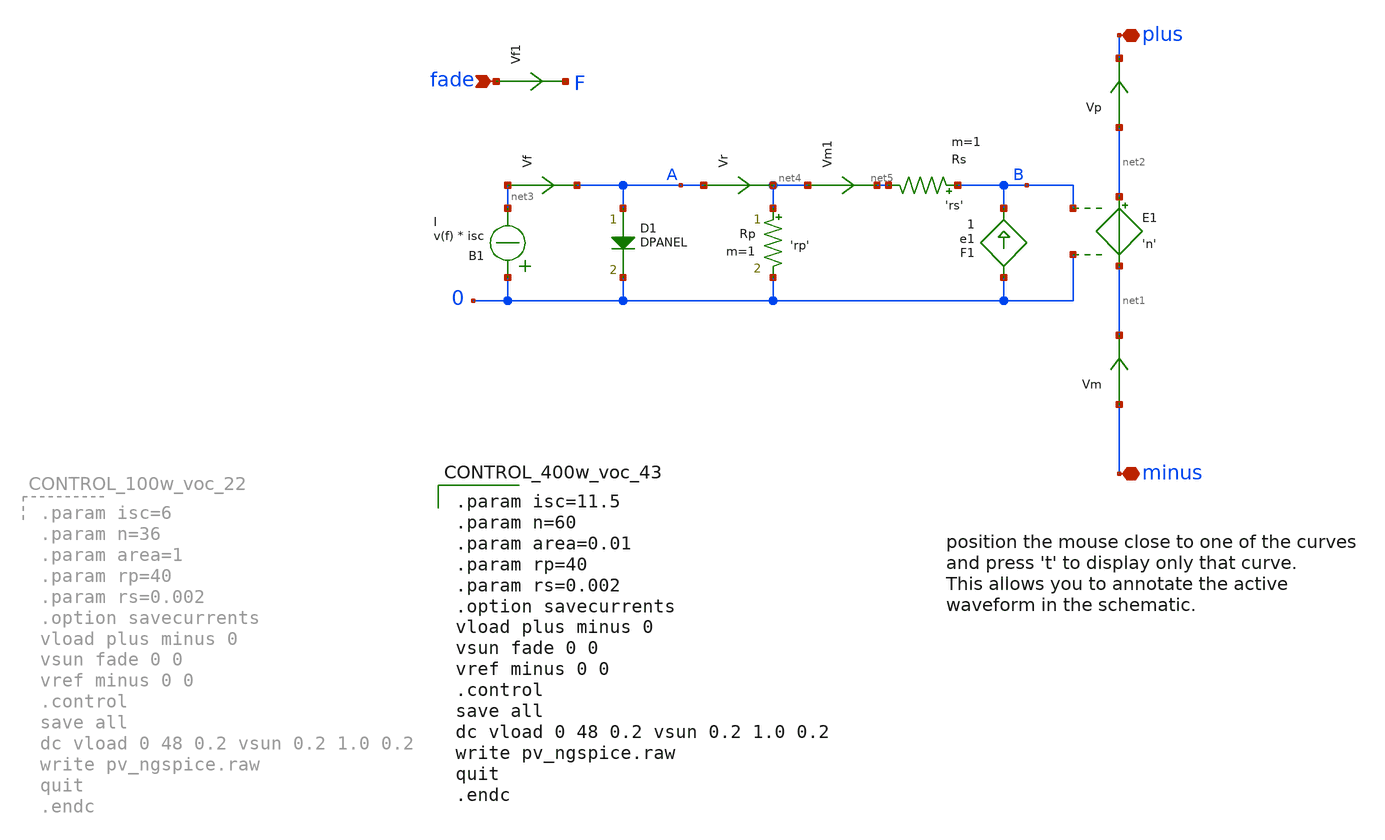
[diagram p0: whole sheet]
** sch_path: xschem_library/ngspice/pv_ngspice.sch
* Copyright (C) 1998-2023 Stefan Frederik Schippers
* This program is free software; you can redistribute it and/or modify
* it under the terms of the GNU General Public License as published by
* the Free Software Foundation; either version 2 of the License, or
* (at your option) any later version.
* This program is distributed in the hope that it will be useful,
* but WITHOUT ANY WARRANTY; without even the implied warranty of
* MERCHANTABILITY or FITNESS FOR A PARTICULAR PURPOSE.  See the
* GNU General Public License for more details.
* You should have received a copy of the GNU General Public License
* along with this program; if not, write to the Free Software
**.subckt pv_ngspice minus fade plus
*.iopin minus
*.ipin fade
*.iopin plus
Vf net3 A 0
.save i(vf)
Vm minus net1 0
.save i(vm)
Vp net2 plus 0
.save i(vp)
D1 A 0 DPANEL area='area'
Rp net4 0 'rp' m=1
Rs B net5 'rs' m=1
F1 0 B e1 1
E1 net2 net1 B 0 'n'
Vf1 fade F 0
.save i(vf1)
B1 0 net3 I = v(f) * isc
Vr A net4 0
.save i(vr)
Vm1 net4 net5 0
.save i(vm1)
**** begin user architecture code

.param isc=11.5
.param n=60
.param area=0.01
.param rp=40
.param rs=0.002
.option savecurrents
vload plus minus 0
vsun fade 0 0
vref minus 0 0
.control
save all
dc vload 0 48 0.2 vsun 0.2 1.0 0.2
write pv_ngspice.raw
quit
.endc


**** end user architecture code
**.ends
**** begin user architecture code
.model DPANEL D IS=1n N=1
**** end user architecture code
.end
